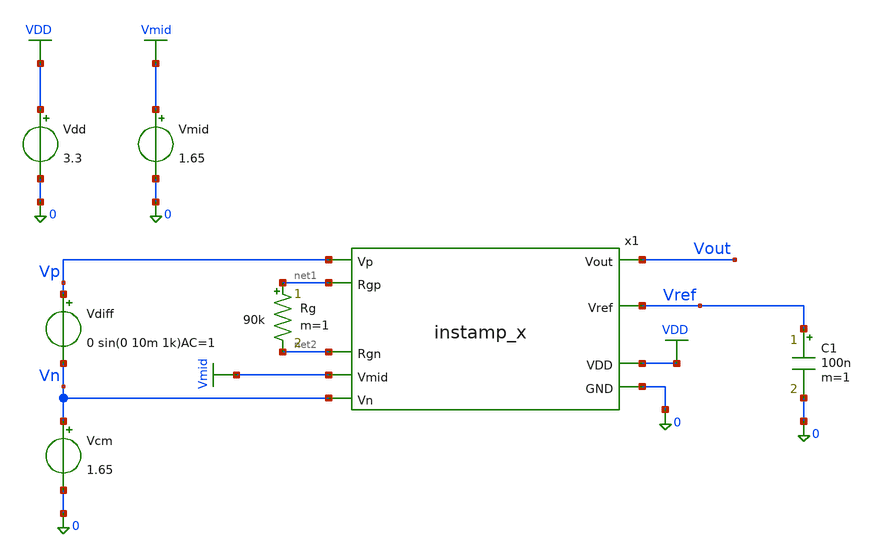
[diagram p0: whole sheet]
** sch_path: xschem/instamp_x_tb.sch
**.subckt instamp_x_tb
x1 Vout Vp VDD net1 0 Vref net2 Vmid Vn instamp_x
Rg net1 net2 90k m=1
Vmid Vmid 0 1.65
Vcm Vn 0 1.65
C1 Vref 0 100n m=1
Vdiff Vp Vn 0 sin(0 10m 1k)AC=1
Vdd VDD 0 3.3
**** begin user architecture code

** opencircuitdesign pdks install
.lib $::SKYWATER_MODELS/sky130.lib.spice tt


.option wnflag=1
.option savecurrents
.save all

.control

* ==========================================
* INITIAL SETUP
* ==========================================

op
write instamp_x_tb.raw
set appendwrite
set gnuplot_terminal=png/quit


* ==========================================
* TRANSIENT ANALYSIS (DISABLED)
* ==========================================

if 0

  destroy all

  foreach val 90k 5k 1k
    alter Rg = $val
    tran 10u 3m 1m
  end

  let Rg90k = tran1.v(vout)
  let Rg5k = tran2.v(vout)
  let Rg1k = tran3.v(vout)

  gnuplot tran Rg90k Rg5k Rg1k  title 'Differential gain'  xlabel 'Time' ylabel 'Volts'

endif


* ==========================================
* SINGLE AC ANALYSIS (DISABLED)
* ==========================================

if 0

  destroy all
  ac dec 100 1 1Meg
  plot db(v(vout))

endif


* ==========================================
* MULTIPLE AC ANALYSES (ENABLED)
* ==========================================

if 1

  destroy all

* ==========================================
* 1. DIFFERENTIAL GAIN ANALYSIS
* ==========================================

  alter vdiff ac=1
  alter vcm ac=0
  alter vdd ac=0
  alter vmid ac=0

  foreach val 90k 5k 1k
    alter Rg = $val
    ac dec 100 1 1Meg
  end


* ==========================================
* 2. COMMON MODE ANALYSIS
* ==========================================

  alter vdiff ac=0
  alter vcm ac=1
  alter vdd ac=0
  alter vmid ac=0

  foreach val 90k 5k 1k
    alter Rg = $val
    ac dec 100 1 1Meg
  end


* ==========================================
* 3. POWER SUPPLY ANALYSIS
* ==========================================

  alter vdiff ac=0
  alter vcm ac=0
  alter vdd ac=1
  alter vmid ac=0

  foreach val 90k 5k 1k
    alter Rg = $val
    ac dec 100 1 1Meg
  end


* ==========================================
* 4. VMID REJECTION ANALYSIS
* ==========================================

  alter vdiff ac=0
  alter vcm ac=0
  alter vdd ac=0
  alter vmid ac=1

  foreach val 90k 5k 1k
    alter Rg = $val
    ac dec 100 1 1Meg
  end


* ==========================================
* 5. CALCULATE DIFFERENTIAL GAIN
* ==========================================

  let Rg90k = db(ac1.v(vout))
  let Rg5k = db(ac2.v(vout))
  let Rg1k = db(ac3.v(vout))


* ==========================================
* 6. CALCULATE CMRR
* ==========================================

  let Rg90k_cm = Rg90k-db(ac4.v(vout))
  let Rg5k_cm = Rg5k-db(ac5.v(vout))
  let Rg1k_cm = Rg1k-db(ac6.v(vout))


* ==========================================
* 7. CALCULATE PSRR
* ==========================================

  let Rg90k_psh = Rg90k-db(ac7.v(vout))
  let Rg5k_psh = Rg5k-db(ac8.v(vout))
  let Rg1k_psh = Rg1k-db(ac9.v(vout))


* ==========================================
* 8. CALCULATE VMID REJECTION
* ==========================================

  let Rg90k_vmid = Rg90k-db(ac10.v(vout))
  let Rg5k_vmid = Rg5k-db(ac11.v(vout))
  let Rg1k_vmid = Rg1k-db(ac12.v(vout))


* ==========================================
* 9. RAW COMMON MODE GAIN
* ==========================================

  let CM90k = db(ac4.v(vout))
  let CM5k = db(ac5.v(vout))
  let CM1k = db(ac6.v(vout))


* ==========================================
* 10. RAW SUPPLY TO OUTPUT GAIN
* ==========================================

  let PS90k = db(ac7.v(vout))
  let PS5k = db(ac8.v(vout))
  let PS1k = db(ac9.v(vout))


* ==========================================
* 11. PRINT CMRR VALUES AT 1 Hz
* ==========================================

  echo ========================================
  echo CMRR VALUES AT 1 Hz
  echo ========================================

  print Rg90k_cm[0]
  print Rg5k_cm[0]
  print Rg1k_cm[0]


* ==========================================
* 12. PRINT PSRR VALUES AT 1 Hz
* ==========================================

  echo ========================================
  echo PSRR VALUES AT 1 Hz
  echo ========================================

  print Rg90k_psh[0]
  print Rg5k_psh[0]
  print Rg1k_psh[0]


* ==========================================
* 13. DIFFERENTIAL GAIN GRAPH
* ==========================================

  gnuplot ac Rg90k Rg5k Rg1k  title 'Differential gain'  xlabel 'Frequency (Hz)' ylabel 'Gain (dB)'


* ==========================================
* 14. CMRR GRAPH
* ==========================================

  gnuplot cmrr Rg90k_cm Rg5k_cm Rg1k_cm  title 'CMRR'  xlabel 'Frequency (Hz)' ylabel 'CMRR (dB)'


* ==========================================
* 15. PSRR GRAPH
* ==========================================

  gnuplot psrr Rg90k_psh Rg5k_psh Rg1k_psh  title 'PSRR'  xlabel 'Frequency (Hz)' ylabel 'PSRR (dB)'


* ==========================================
* 16. VMID REJECTION GRAPH
* ==========================================

  gnuplot vmid_rej Rg90k_vmid Rg5k_vmid Rg1k_vmid  title 'Vmid Rejection'  xlabel 'Frequency (Hz)' ylabel
+ 'Rejection (dB)'


* ==========================================
* 17. RAW COMMON MODE GAIN GRAPH (NEW)
* ==========================================

  gnuplot cm_gain CM90k CM5k CM1k  title 'Common Mode Gain'  xlabel 'Frequency (Hz)' ylabel 'Gain (dB)'


* ==========================================
* 18. RAW SUPPLY GAIN GRAPH (NEW)
* ==========================================

  gnuplot supply_gain PS90k PS5k PS1k  title 'Supply to Output Gain'  xlabel 'Frequency (Hz)' ylabel
+ 'Gain (dB)'


endif

.endc

**** end user architecture code
**.ends

* expanding   symbol:  instamp_x.sym # of pins=9
** sym_path: xschem/instamp_x.sym
** sch_path: xschem/instamp_x.sch
.subckt instamp_x Vout Vp VDD Rgp GND Vref Rgn Vmid Vn
*.ipin VDD
*.ipin GND
*.opin Vout
*.ipin Vn
*.ipin Vp
*.ipin Rgn
*.ipin Rgp
*.opin Vref
*.ipin Vmid
x1 VDD Vp Rgp Vout Vref GND opamp_x
x2 VDD Vn Rgn net1 Vref GND opamp_x
R1 Rgp Vout 40k m=1
R2 Rgp net1 10.1k m=1
R3 Rgn net1 10k m=1
R4 Vmid Rgn 40k m=1
x3 VDD Vref GND bandgap_x
.ends


* expanding   symbol:  opamp_x.sym # of pins=6
** sym_path: xschem/opamp_x.sym
** sch_path: xschem/opamp_x.sch
.subckt opamp_x VDD Vp Vn Vout Vref GND
*.ipin Vref
*.ipin Vn
*.ipin Vp
*.opin Vout
*.ipin VDD
*.ipin GND
XM1 net3 net3 net1 GND sky130_fd_pr__nfet_g5v0d10v5 L=2 W=3.33 nf=1 ad='int((1 + 1)/2) * 3.33 / 1 * 0.29'
+ as='int((1 + 2)/2) * 3.33 / 1 * 0.29' pd='2*int((1 + 1)/2) * (3.33 / 1 + 0.29)' ps='2*int((1 + 2)/2) * (3.33 / 1 + 0.29)'
+ nrd='0.29 / 3.33 ' nrs='0.29 / 3.33 ' sa=0 sb=0 sd=0 mult=3 m=3
XM2 net1 net3 GND GND sky130_fd_pr__nfet_g5v0d10v5 L=5 W=5 nf=1 ad='int((1 + 1)/2) * 5 / 1 * 0.29' as='int((1 + 2)/2) * 5 / 1 * 0.29'
+ pd='2*int((1 + 1)/2) * (5 / 1 + 0.29)' ps='2*int((1 + 2)/2) * (5 / 1 + 0.29)' nrd='0.29 / 5 ' nrs='0.29 / 5 '
+ sa=0 sb=0 sd=0 mult=1 m=1
XM3 net2 net3 net4 GND sky130_fd_pr__nfet_g5v0d10v5 L=2 W=3.33 nf=1 ad='int((1 + 1)/2) * 3.33 / 1 * 0.29'
+ as='int((1 + 2)/2) * 3.33 / 1 * 0.29' pd='2*int((1 + 1)/2) * (3.33 / 1 + 0.29)' ps='2*int((1 + 2)/2) * (3.33 / 1 + 0.29)'
+ nrd='0.29 / 3.33 ' nrs='0.29 / 3.33 ' sa=0 sb=0 sd=0 mult=3 m=3
XM4 net4 net3 GND GND sky130_fd_pr__nfet_g5v0d10v5 L=5 W=5 nf=1 ad='int((1 + 1)/2) * 5 / 1 * 0.29' as='int((1 + 2)/2) * 5 / 1 * 0.29'
+ pd='2*int((1 + 1)/2) * (5 / 1 + 0.29)' ps='2*int((1 + 2)/2) * (5 / 1 + 0.29)' nrd='0.29 / 5 ' nrs='0.29 / 5 '
+ sa=0 sb=0 sd=0 mult=1 m=1
XM5 net5 net2 VDD VDD sky130_fd_pr__pfet_g5v0d10v5 L=1 W=3 nf=1 ad='int((1 + 1)/2) * 3 / 1 * 0.29' as='int((1 + 2)/2) * 3 / 1 * 0.29'
+ pd='2*int((1 + 1)/2) * (3 / 1 + 0.29)' ps='2*int((1 + 2)/2) * (3 / 1 + 0.29)' nrd='0.29 / 3 ' nrs='0.29 / 3 '
+ sa=0 sb=0 sd=0 mult=1 m=1
XM6 net2 net2 net5 VDD sky130_fd_pr__pfet_g5v0d10v5 L=1 W=10 nf=1 ad='int((1 + 1)/2) * 10 / 1 * 0.29'
+ as='int((1 + 2)/2) * 10 / 1 * 0.29' pd='2*int((1 + 1)/2) * (10 / 1 + 0.29)' ps='2*int((1 + 2)/2) * (10 / 1 + 0.29)'
+ nrd='0.29 / 10 ' nrs='0.29 / 10 ' sa=0 sb=0 sd=0 mult=1 m=1
XM7 net6 net2 VDD VDD sky130_fd_pr__pfet_g5v0d10v5 L=1 W=1 nf=1 ad='int((1 + 1)/2) * 1 / 1 * 0.29' as='int((1 + 2)/2) * 1 / 1 * 0.29'
+ pd='2*int((1 + 1)/2) * (1 / 1 + 0.29)' ps='2*int((1 + 2)/2) * (1 / 1 + 0.29)' nrd='0.29 / 1 ' nrs='0.29 / 1 '
+ sa=0 sb=0 sd=0 mult=3 m=3
XM8 net7 net2 net6 VDD sky130_fd_pr__pfet_g5v0d10v5 L=0.5 W=10 nf=1 ad='int((1 + 1)/2) * 10 / 1 * 0.29'
+ as='int((1 + 2)/2) * 10 / 1 * 0.29' pd='2*int((1 + 1)/2) * (10 / 1 + 0.29)' ps='2*int((1 + 2)/2) * (10 / 1 + 0.29)'
+ nrd='0.29 / 10 ' nrs='0.29 / 10 ' sa=0 sb=0 sd=0 mult=1 m=1
XM9 net13 Vp net7 VDD sky130_fd_pr__pfet_g5v0d10v5 L=3 W=20 nf=1 ad='int((1 + 1)/2) * 20 / 1 * 0.29'
+ as='int((1 + 2)/2) * 20 / 1 * 0.29' pd='2*int((1 + 1)/2) * (20 / 1 + 0.29)' ps='2*int((1 + 2)/2) * (20 / 1 + 0.29)'
+ nrd='0.29 / 20 ' nrs='0.29 / 20 ' sa=0 sb=0 sd=0 mult=10 m=10
XM10 net12 Vn net7 VDD sky130_fd_pr__pfet_g5v0d10v5 L=3 W=20 nf=1 ad='int((1 + 1)/2) * 20 / 1 * 0.29'
+ as='int((1 + 2)/2) * 20 / 1 * 0.29' pd='2*int((1 + 1)/2) * (20 / 1 + 0.29)' ps='2*int((1 + 2)/2) * (20 / 1 + 0.29)'
+ nrd='0.29 / 20 ' nrs='0.29 / 20 ' sa=0 sb=0 sd=0 mult=10 m=10
XM11 net10 net9 VDD VDD sky130_fd_pr__pfet_g5v0d10v5 L=5 W=20 nf=1 ad='int((1 + 1)/2) * 20 / 1 * 0.29'
+ as='int((1 + 2)/2) * 20 / 1 * 0.29' pd='2*int((1 + 1)/2) * (20 / 1 + 0.29)' ps='2*int((1 + 2)/2) * (20 / 1 + 0.29)'
+ nrd='0.29 / 20 ' nrs='0.29 / 20 ' sa=0 sb=0 sd=0 mult=5 m=5
XM12 net9 net9 net10 VDD sky130_fd_pr__pfet_g5v0d10v5 L=2 W=20 nf=1 ad='int((1 + 1)/2) * 20 / 1 * 0.29'
+ as='int((1 + 2)/2) * 20 / 1 * 0.29' pd='2*int((1 + 1)/2) * (20 / 1 + 0.29)' ps='2*int((1 + 2)/2) * (20 / 1 + 0.29)'
+ nrd='0.29 / 20 ' nrs='0.29 / 20 ' sa=0 sb=0 sd=0 mult=5 m=5
XM13 net11 net9 VDD VDD sky130_fd_pr__pfet_g5v0d10v5 L=5 W=20 nf=1 ad='int((1 + 1)/2) * 20 / 1 * 0.29'
+ as='int((1 + 2)/2) * 20 / 1 * 0.29' pd='2*int((1 + 1)/2) * (20 / 1 + 0.29)' ps='2*int((1 + 2)/2) * (20 / 1 + 0.29)'
+ nrd='0.29 / 20 ' nrs='0.29 / 20 ' sa=0 sb=0 sd=0 mult=5 m=5
XM14 net18 net9 net11 VDD sky130_fd_pr__pfet_g5v0d10v5 L=2 W=20 nf=1 ad='int((1 + 1)/2) * 20 / 1 * 0.29'
+ as='int((1 + 2)/2) * 20 / 1 * 0.29' pd='2*int((1 + 1)/2) * (20 / 1 + 0.29)' ps='2*int((1 + 2)/2) * (20 / 1 + 0.29)'
+ nrd='0.29 / 20 ' nrs='0.29 / 20 ' sa=0 sb=0 sd=0 mult=5 m=5
XM15 net9 net3 net12 GND sky130_fd_pr__nfet_g5v0d10v5 L=2 W=20 nf=1 ad='int((1 + 1)/2) * 20 / 1 * 0.29'
+ as='int((1 + 2)/2) * 20 / 1 * 0.29' pd='2*int((1 + 1)/2) * (20 / 1 + 0.29)' ps='2*int((1 + 2)/2) * (20 / 1 + 0.29)'
+ nrd='0.29 / 20 ' nrs='0.29 / 20 ' sa=0 sb=0 sd=0 mult=5 m=5
XM16 net12 net3 GND GND sky130_fd_pr__nfet_g5v0d10v5 L=5 W=10 nf=1 ad='int((1 + 1)/2) * 10 / 1 * 0.29'
+ as='int((1 + 2)/2) * 10 / 1 * 0.29' pd='2*int((1 + 1)/2) * (10 / 1 + 0.29)' ps='2*int((1 + 2)/2) * (10 / 1 + 0.29)'
+ nrd='0.29 / 10 ' nrs='0.29 / 10 ' sa=0 sb=0 sd=0 mult=1 m=1
XM17 net17 net3 net13 GND sky130_fd_pr__nfet_g5v0d10v5 L=2 W=20 nf=1 ad='int((1 + 1)/2) * 20 / 1 * 0.29'
+ as='int((1 + 2)/2) * 20 / 1 * 0.29' pd='2*int((1 + 1)/2) * (20 / 1 + 0.29)' ps='2*int((1 + 2)/2) * (20 / 1 + 0.29)'
+ nrd='0.29 / 20 ' nrs='0.29 / 20 ' sa=0 sb=0 sd=0 mult=5 m=5
XM18 net13 net3 GND GND sky130_fd_pr__nfet_g5v0d10v5 L=5 W=10 nf=1 ad='int((1 + 1)/2) * 10 / 1 * 0.29'
+ as='int((1 + 2)/2) * 10 / 1 * 0.29' pd='2*int((1 + 1)/2) * (10 / 1 + 0.29)' ps='2*int((1 + 2)/2) * (10 / 1 + 0.29)'
+ nrd='0.29 / 10 ' nrs='0.29 / 10 ' sa=0 sb=0 sd=0 mult=1 m=1
XM19 net17 net14 net18 VDD sky130_fd_pr__pfet_g5v0d10v5 L=0.5 W=15 nf=1 ad='int((1 + 1)/2) * 15 / 1 * 0.29'
+ as='int((1 + 2)/2) * 15 / 1 * 0.29' pd='2*int((1 + 1)/2) * (15 / 1 + 0.29)' ps='2*int((1 + 2)/2) * (15 / 1 + 0.29)'
+ nrd='0.29 / 15 ' nrs='0.29 / 15 ' sa=0 sb=0 sd=0 mult=10 m=10
XM20 net14 net3 GND GND sky130_fd_pr__nfet_g5v0d10v5 L=5 W=1.5 nf=1 ad='int((1 + 1)/2) * 1.5 / 1 * 0.29'
+ as='int((1 + 2)/2) * 1.5 / 1 * 0.29' pd='2*int((1 + 1)/2) * (1.5 / 1 + 0.29)' ps='2*int((1 + 2)/2) * (1.5 / 1 + 0.29)'
+ nrd='0.29 / 1.5 ' nrs='0.29 / 1.5 ' sa=0 sb=0 sd=0 mult=1 m=1
XM21 net15 net15 VDD VDD sky130_fd_pr__pfet_g5v0d10v5 L=10 W=15 nf=1 ad='int((1 + 1)/2) * 15 / 1 * 0.29'
+ as='int((1 + 2)/2) * 15 / 1 * 0.29' pd='2*int((1 + 1)/2) * (15 / 1 + 0.29)' ps='2*int((1 + 2)/2) * (15 / 1 + 0.29)'
+ nrd='0.29 / 15 ' nrs='0.29 / 15 ' sa=0 sb=0 sd=0 mult=10 m=10
XM22 net14 net14 net15 VDD sky130_fd_pr__pfet_g5v0d10v5 L=10 W=15 nf=1 ad='int((1 + 1)/2) * 15 / 1 * 0.29'
+ as='int((1 + 2)/2) * 15 / 1 * 0.29' pd='2*int((1 + 1)/2) * (15 / 1 + 0.29)' ps='2*int((1 + 2)/2) * (15 / 1 + 0.29)'
+ nrd='0.29 / 15 ' nrs='0.29 / 15 ' sa=0 sb=0 sd=0 mult=10 m=10
XM24 net16 net2 VDD VDD sky130_fd_pr__pfet_g5v0d10v5 L=5 W=4 nf=1 ad='int((1 + 1)/2) * 4 / 1 * 0.29'
+ as='int((1 + 2)/2) * 4 / 1 * 0.29' pd='2*int((1 + 1)/2) * (4 / 1 + 0.29)' ps='2*int((1 + 2)/2) * (4 / 1 + 0.29)'
+ nrd='0.29 / 4 ' nrs='0.29 / 4 ' sa=0 sb=0 sd=0 mult=1 m=1
XM25 net16 net16 net19 GND sky130_fd_pr__nfet_g5v0d10v5 L=0.5 W=15 nf=1 ad='int((1 + 1)/2) * 15 / 1 * 0.29'
+ as='int((1 + 2)/2) * 15 / 1 * 0.29' pd='2*int((1 + 1)/2) * (15 / 1 + 0.29)' ps='2*int((1 + 2)/2) * (15 / 1 + 0.29)'
+ nrd='0.29 / 15 ' nrs='0.29 / 15 ' sa=0 sb=0 sd=0 mult=7 m=7
XM26 net19 net19 GND GND sky130_fd_pr__nfet_g5v0d10v5 L=0.5 W=15 nf=1 ad='int((1 + 1)/2) * 15 / 1 * 0.29'
+ as='int((1 + 2)/2) * 15 / 1 * 0.29' pd='2*int((1 + 1)/2) * (15 / 1 + 0.29)' ps='2*int((1 + 2)/2) * (15 / 1 + 0.29)'
+ nrd='0.29 / 15 ' nrs='0.29 / 15 ' sa=0 sb=0 sd=0 mult=7 m=7
XM27 Vout net18 VDD VDD sky130_fd_pr__pfet_g5v0d10v5 L=0.5 W=20 nf=1 ad='int((1 + 1)/2) * 20 / 1 * 0.29'
+ as='int((1 + 2)/2) * 20 / 1 * 0.29' pd='2*int((1 + 1)/2) * (20 / 1 + 0.29)' ps='2*int((1 + 2)/2) * (20 / 1 + 0.29)'
+ nrd='0.29 / 20 ' nrs='0.29 / 20 ' sa=0 sb=0 sd=0 mult=20 m=20
XM28 Vout net17 GND GND sky130_fd_pr__nfet_g5v0d10v5 L=0.5 W=10 nf=1 ad='int((1 + 1)/2) * 10 / 1 * 0.29'
+ as='int((1 + 2)/2) * 10 / 1 * 0.29' pd='2*int((1 + 1)/2) * (10 / 1 + 0.29)' ps='2*int((1 + 2)/2) * (10 / 1 + 0.29)'
+ nrd='0.29 / 10 ' nrs='0.29 / 10 ' sa=0 sb=0 sd=0 mult=10 m=10
XM33 net11 Vp net8 GND sky130_fd_pr__nfet_g5v0d10v5 L=2 W=20 nf=1 ad='int((1 + 1)/2) * 20 / 1 * 0.29'
+ as='int((1 + 2)/2) * 20 / 1 * 0.29' pd='2*int((1 + 1)/2) * (20 / 1 + 0.29)' ps='2*int((1 + 2)/2) * (20 / 1 + 0.29)'
+ nrd='0.29 / 20 ' nrs='0.29 / 20 ' sa=0 sb=0 sd=0 mult=5 m=5
XM30 net10 Vn net8 GND sky130_fd_pr__nfet_g5v0d10v5 L=2 W=20 nf=1 ad='int((1 + 1)/2) * 20 / 1 * 0.29'
+ as='int((1 + 2)/2) * 20 / 1 * 0.29' pd='2*int((1 + 1)/2) * (20 / 1 + 0.29)' ps='2*int((1 + 2)/2) * (20 / 1 + 0.29)'
+ nrd='0.29 / 20 ' nrs='0.29 / 20 ' sa=0 sb=0 sd=0 mult=5 m=5
XM31 net8 net3 net22 GND sky130_fd_pr__nfet_g5v0d10v5 L=2 W=20 nf=1 ad='int((1 + 1)/2) * 20 / 1 * 0.29'
+ as='int((1 + 2)/2) * 20 / 1 * 0.29' pd='2*int((1 + 1)/2) * (20 / 1 + 0.29)' ps='2*int((1 + 2)/2) * (20 / 1 + 0.29)'
+ nrd='0.29 / 20 ' nrs='0.29 / 20 ' sa=0 sb=0 sd=0 mult=1 m=1
XM32 net22 net3 GND GND sky130_fd_pr__nfet_g5v0d10v5 L=5 W=10 nf=1 ad='int((1 + 1)/2) * 10 / 1 * 0.29'
+ as='int((1 + 2)/2) * 10 / 1 * 0.29' pd='2*int((1 + 1)/2) * (10 / 1 + 0.29)' ps='2*int((1 + 2)/2) * (10 / 1 + 0.29)'
+ nrd='0.29 / 10 ' nrs='0.29 / 10 ' sa=0 sb=0 sd=0 mult=1 m=1
XM23 net18 net16 net17 GND sky130_fd_pr__nfet_g5v0d10v5 L=0.5 W=10 nf=1 ad='int((1 + 1)/2) * 10 / 1 * 0.29'
+ as='int((1 + 2)/2) * 10 / 1 * 0.29' pd='2*int((1 + 1)/2) * (10 / 1 + 0.29)' ps='2*int((1 + 2)/2) * (10 / 1 + 0.29)'
+ nrd='0.29 / 10 ' nrs='0.29 / 10 ' sa=0 sb=0 sd=0 mult=5 m=5
XMr1 net21 Vref GND GND sky130_fd_pr__nfet_g5v0d10v5 L=7 W=5 nf=1 ad='int((1 + 1)/2) * 5 / 1 * 0.29'
+ as='int((1 + 2)/2) * 5 / 1 * 0.29' pd='2*int((1 + 1)/2) * (5 / 1 + 0.29)' ps='2*int((1 + 2)/2) * (5 / 1 + 0.29)'
+ nrd='0.29 / 5 ' nrs='0.29 / 5 ' sa=0 sb=0 sd=0 mult=1 m=1
XMr2 net20 net20 VDD VDD sky130_fd_pr__pfet_g5v0d10v5 L=1 W=1 nf=1 ad='int((1 + 1)/2) * 1 / 1 * 0.29'
+ as='int((1 + 2)/2) * 1 / 1 * 0.29' pd='2*int((1 + 1)/2) * (1 / 1 + 0.29)' ps='2*int((1 + 2)/2) * (1 / 1 + 0.29)'
+ nrd='0.29 / 1 ' nrs='0.29 / 1 ' sa=0 sb=0 sd=0 mult=1 m=1
XMr3 net3 net20 VDD VDD sky130_fd_pr__pfet_g5v0d10v5 L=1 W=1 nf=1 ad='int((1 + 1)/2) * 1 / 1 * 0.29'
+ as='int((1 + 2)/2) * 1 / 1 * 0.29' pd='2*int((1 + 1)/2) * (1 / 1 + 0.29)' ps='2*int((1 + 2)/2) * (1 / 1 + 0.29)'
+ nrd='0.29 / 1 ' nrs='0.29 / 1 ' sa=0 sb=0 sd=0 mult=1 m=1
Vmeas_Iref net20 net21 0
.save i(vmeas_iref)
XC2 Vout net17 sky130_fd_pr__cap_mim_m3_2 W=25 L=25 MF=4 m=4
XC1 net18 Vout sky130_fd_pr__cap_mim_m3_2 W=25 L=25 MF=4 m=4
.ends


* expanding   symbol:  bandgap_x.sym # of pins=3
** sym_path: xschem/bandgap_x.sym
** sch_path: xschem/bandgap_x.sch
.subckt bandgap_x VDD Vref GND
*.opin Vref
*.ipin GND
*.ipin VDD
XM2 Vg3 Vg2 net1 net1 sky130_fd_pr__pfet_g5v0d10v5 L=1 W=20 nf=1 ad='int((1 + 1)/2) * 20 / 1 * 0.29'
+ as='int((1 + 2)/2) * 20 / 1 * 0.29' pd='2*int((1 + 1)/2) * (20 / 1 + 0.29)' ps='2*int((1 + 2)/2) * (20 / 1 + 0.29)'
+ nrd='0.29 / 20 ' nrs='0.29 / 20 ' sa=0 sb=0 sd=0 mult=1 m=1
XM1 Vg10 Vg1 net1 net1 sky130_fd_pr__pfet_g5v0d10v5 L=1 W=20 nf=1 ad='int((1 + 1)/2) * 20 / 1 * 0.29'
+ as='int((1 + 2)/2) * 20 / 1 * 0.29' pd='2*int((1 + 1)/2) * (20 / 1 + 0.29)' ps='2*int((1 + 2)/2) * (20 / 1 + 0.29)'
+ nrd='0.29 / 20 ' nrs='0.29 / 20 ' sa=0 sb=0 sd=0 mult=1 m=1
XM3 Vg10 Vg3 GND GND sky130_fd_pr__nfet_g5v0d10v5 L=1 W=20 nf=1 ad='int((1 + 1)/2) * 20 / 1 * 0.29' as='int((1 + 2)/2) * 20 / 1 * 0.29'
+ pd='2*int((1 + 1)/2) * (20 / 1 + 0.29)' ps='2*int((1 + 2)/2) * (20 / 1 + 0.29)' nrd='0.29 / 20 ' nrs='0.29 / 20 '
+ sa=0 sb=0 sd=0 mult=1 m=1
XM4 Vg3 Vg3 GND GND sky130_fd_pr__nfet_g5v0d10v5 L=1 W=20 nf=1 ad='int((1 + 1)/2) * 20 / 1 * 0.29' as='int((1 + 2)/2) * 20 / 1 * 0.29'
+ pd='2*int((1 + 1)/2) * (20 / 1 + 0.29)' ps='2*int((1 + 2)/2) * (20 / 1 + 0.29)' nrd='0.29 / 20 ' nrs='0.29 / 20 '
+ sa=0 sb=0 sd=0 mult=1 m=1
XM5 Vg5 Vg5 VDD VDD sky130_fd_pr__pfet_g5v0d10v5 L=1 W=1 nf=1 ad='int((1 + 1)/2) * 1 / 1 * 0.29' as='int((1 + 2)/2) * 1 / 1 * 0.29'
+ pd='2*int((1 + 1)/2) * (1 / 1 + 0.29)' ps='2*int((1 + 2)/2) * (1 / 1 + 0.29)' nrd='0.29 / 1 ' nrs='0.29 / 1 '
+ sa=0 sb=0 sd=0 mult=1 m=1
XM6 Vg5 Vref Vs5 GND sky130_fd_pr__nfet_g5v0d10v5 L=1 W=5 nf=1 ad='int((1 + 1)/2) * 5 / 1 * 0.29' as='int((1 + 2)/2) * 5 / 1 * 0.29'
+ pd='2*int((1 + 1)/2) * (5 / 1 + 0.29)' ps='2*int((1 + 2)/2) * (5 / 1 + 0.29)' nrd='0.29 / 5 ' nrs='0.29 / 5 '
+ sa=0 sb=0 sd=0 mult=1 m=1
XM7a Vg12 Vg12 net3 GND sky130_fd_pr__nfet_g5v0d10v5 L=10 W=0.5 nf=1 ad='int((1 + 1)/2) * 0.5 / 1 * 0.29'
+ as='int((1 + 2)/2) * 0.5 / 1 * 0.29' pd='2*int((1 + 1)/2) * (0.5 / 1 + 0.29)' ps='2*int((1 + 2)/2) * (0.5 / 1 + 0.29)'
+ nrd='0.29 / 0.5 ' nrs='0.29 / 0.5 ' sa=0 sb=0 sd=0 mult=1 m=1
XM8 Vg12 Vg5 VDD VDD sky130_fd_pr__pfet_g5v0d10v5 L=1 W=1 nf=1 ad='int((1 + 1)/2) * 1 / 1 * 0.29' as='int((1 + 2)/2) * 1 / 1 * 0.29'
+ pd='2*int((1 + 1)/2) * (1 / 1 + 0.29)' ps='2*int((1 + 2)/2) * (1 / 1 + 0.29)' nrd='0.29 / 1 ' nrs='0.29 / 1 '
+ sa=0 sb=0 sd=0 mult=1 m=1
XM9 Vg12 Vref net2 GND sky130_fd_pr__nfet_g5v0d10v5 L=1 W=20 nf=1 ad='int((1 + 1)/2) * 20 / 1 * 0.29'
+ as='int((1 + 2)/2) * 20 / 1 * 0.29' pd='2*int((1 + 1)/2) * (20 / 1 + 0.29)' ps='2*int((1 + 2)/2) * (20 / 1 + 0.29)'
+ nrd='0.29 / 20 ' nrs='0.29 / 20 ' sa=0 sb=0 sd=0 mult=1 m=1
XM10 net2 Vg10 GND GND sky130_fd_pr__nfet_g5v0d10v5 L=1 W=20 nf=1 ad='int((1 + 1)/2) * 20 / 1 * 0.29'
+ as='int((1 + 2)/2) * 20 / 1 * 0.29' pd='2*int((1 + 1)/2) * (20 / 1 + 0.29)' ps='2*int((1 + 2)/2) * (20 / 1 + 0.29)'
+ nrd='0.29 / 20 ' nrs='0.29 / 20 ' sa=0 sb=0 sd=0 mult=1 m=1
XM11 net1 Vg5 VDD VDD sky130_fd_pr__pfet_g5v0d10v5 L=1 W=1 nf=1 ad='int((1 + 1)/2) * 1 / 1 * 0.29' as='int((1 + 2)/2) * 1 / 1 * 0.29'
+ pd='2*int((1 + 1)/2) * (1 / 1 + 0.29)' ps='2*int((1 + 2)/2) * (1 / 1 + 0.29)' nrd='0.29 / 1 ' nrs='0.29 / 1 '
+ sa=0 sb=0 sd=0 mult=1 m=1
XM12 Vref Vg12 VDD VDD sky130_fd_pr__pfet_g5v0d10v5 L=0.5 W=20 nf=1 ad='int((1 + 1)/2) * 20 / 1 * 0.29'
+ as='int((1 + 2)/2) * 20 / 1 * 0.29' pd='2*int((1 + 1)/2) * (20 / 1 + 0.29)' ps='2*int((1 + 2)/2) * (20 / 1 + 0.29)'
+ nrd='0.29 / 20 ' nrs='0.29 / 20 ' sa=0 sb=0 sd=0 mult=1 m=1
XR1 Vg2 Vref GND sky130_fd_pr__res_high_po_0p35 L=21.3 mult=1 m=1
XR2 Vg1 Vref GND sky130_fd_pr__res_high_po_0p35 L=21.3 mult=1 m=1
XR3 Ve1 Vg1 GND sky130_fd_pr__res_high_po_0p35 L=3 mult=1 m=1
XR4 GND Vs5 GND sky130_fd_pr__res_high_po_0p35 L=47.02 mult=1 m=1
XQ1 GND GND Ve1 sky130_fd_pr__pnp_05v5_W3p40L3p40 m=24
XQ2 GND GND Vg2 sky130_fd_pr__pnp_05v5_W3p40L3p40 m=1
XM7b net3 Vg12 net4 GND sky130_fd_pr__nfet_g5v0d10v5 L=10 W=0.5 nf=1 ad='int((1 + 1)/2) * 0.5 / 1 * 0.29'
+ as='int((1 + 2)/2) * 0.5 / 1 * 0.29' pd='2*int((1 + 1)/2) * (0.5 / 1 + 0.29)' ps='2*int((1 + 2)/2) * (0.5 / 1 + 0.29)'
+ nrd='0.29 / 0.5 ' nrs='0.29 / 0.5 ' sa=0 sb=0 sd=0 mult=1 m=1
XM7c net4 Vg12 net5 GND sky130_fd_pr__nfet_g5v0d10v5 L=10 W=0.5 nf=1 ad='int((1 + 1)/2) * 0.5 / 1 * 0.29'
+ as='int((1 + 2)/2) * 0.5 / 1 * 0.29' pd='2*int((1 + 1)/2) * (0.5 / 1 + 0.29)' ps='2*int((1 + 2)/2) * (0.5 / 1 + 0.29)'
+ nrd='0.29 / 0.5 ' nrs='0.29 / 0.5 ' sa=0 sb=0 sd=0 mult=1 m=1
XM7d net5 Vg12 net6 GND sky130_fd_pr__nfet_g5v0d10v5 L=10 W=0.5 nf=1 ad='int((1 + 1)/2) * 0.5 / 1 * 0.29'
+ as='int((1 + 2)/2) * 0.5 / 1 * 0.29' pd='2*int((1 + 1)/2) * (0.5 / 1 + 0.29)' ps='2*int((1 + 2)/2) * (0.5 / 1 + 0.29)'
+ nrd='0.29 / 0.5 ' nrs='0.29 / 0.5 ' sa=0 sb=0 sd=0 mult=1 m=1
XM7e net6 Vg12 net7 GND sky130_fd_pr__nfet_g5v0d10v5 L=10 W=0.5 nf=1 ad='int((1 + 1)/2) * 0.5 / 1 * 0.29'
+ as='int((1 + 2)/2) * 0.5 / 1 * 0.29' pd='2*int((1 + 1)/2) * (0.5 / 1 + 0.29)' ps='2*int((1 + 2)/2) * (0.5 / 1 + 0.29)'
+ nrd='0.29 / 0.5 ' nrs='0.29 / 0.5 ' sa=0 sb=0 sd=0 mult=1 m=1
XM7 net7 Vg12 net8 GND sky130_fd_pr__nfet_g5v0d10v5 L=10 W=0.5 nf=1 ad='int((1 + 1)/2) * 0.5 / 1 * 0.29'
+ as='int((1 + 2)/2) * 0.5 / 1 * 0.29' pd='2*int((1 + 1)/2) * (0.5 / 1 + 0.29)' ps='2*int((1 + 2)/2) * (0.5 / 1 + 0.29)'
+ nrd='0.29 / 0.5 ' nrs='0.29 / 0.5 ' sa=0 sb=0 sd=0 mult=1 m=1
XM13 net8 Vg12 net9 GND sky130_fd_pr__nfet_g5v0d10v5 L=10 W=0.5 nf=1 ad='int((1 + 1)/2) * 0.5 / 1 * 0.29'
+ as='int((1 + 2)/2) * 0.5 / 1 * 0.29' pd='2*int((1 + 1)/2) * (0.5 / 1 + 0.29)' ps='2*int((1 + 2)/2) * (0.5 / 1 + 0.29)'
+ nrd='0.29 / 0.5 ' nrs='0.29 / 0.5 ' sa=0 sb=0 sd=0 mult=1 m=1
XM14 net9 Vg12 net10 GND sky130_fd_pr__nfet_g5v0d10v5 L=10 W=0.5 nf=1 ad='int((1 + 1)/2) * 0.5 / 1 * 0.29'
+ as='int((1 + 2)/2) * 0.5 / 1 * 0.29' pd='2*int((1 + 1)/2) * (0.5 / 1 + 0.29)' ps='2*int((1 + 2)/2) * (0.5 / 1 + 0.29)'
+ nrd='0.29 / 0.5 ' nrs='0.29 / 0.5 ' sa=0 sb=0 sd=0 mult=1 m=1
XM15 net10 Vg12 net11 GND sky130_fd_pr__nfet_g5v0d10v5 L=10 W=0.5 nf=1 ad='int((1 + 1)/2) * 0.5 / 1 * 0.29'
+ as='int((1 + 2)/2) * 0.5 / 1 * 0.29' pd='2*int((1 + 1)/2) * (0.5 / 1 + 0.29)' ps='2*int((1 + 2)/2) * (0.5 / 1 + 0.29)'
+ nrd='0.29 / 0.5 ' nrs='0.29 / 0.5 ' sa=0 sb=0 sd=0 mult=1 m=1
XM16 net11 Vg12 GND GND sky130_fd_pr__nfet_g5v0d10v5 L=10 W=0.5 nf=1 ad='int((1 + 1)/2) * 0.5 / 1 * 0.29'
+ as='int((1 + 2)/2) * 0.5 / 1 * 0.29' pd='2*int((1 + 1)/2) * (0.5 / 1 + 0.29)' ps='2*int((1 + 2)/2) * (0.5 / 1 + 0.29)'
+ nrd='0.29 / 0.5 ' nrs='0.29 / 0.5 ' sa=0 sb=0 sd=0 mult=1 m=1
.ends

.GLOBAL Vmid
.GLOBAL VDD
.end
